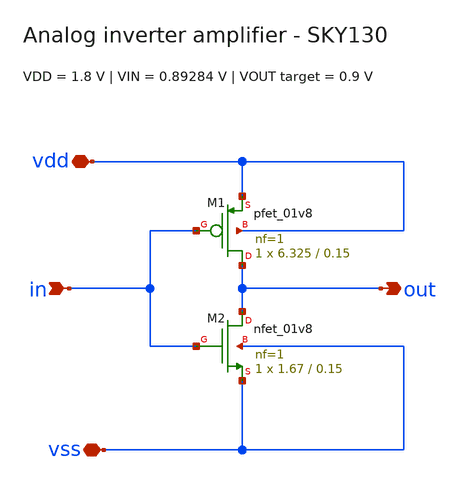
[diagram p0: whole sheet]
** sch_path: ISSCC27/submitted_notebooks/PerfPDN/examples/inverter_amplifier/inv.sch
**.subckt inv in out vdd vss
*.ipin in
*.opin out
*.iopin vdd
*.iopin vss
XM1 out in vdd vdd sky130_fd_pr__pfet_01v8 L=0.15 W=6.325 nf=1 ad='int(( 1 + 1 ) / 2 ) * 6.325 / 1 * 0.29'
+ as='int(( 1 + 2 ) / 2 ) * 6.325 / 1 * 0.29' pd='2 * int(( 1 + 1 ) / 2 ) * ( 6.325 / 1 + 0.29 )' ps='2 * int(( 1 + 2 ) / 2 ) * ( 6.325 / 1 + 0.29 )'
+ nrd='0.29 / 6.325 ' nrs='0.29 / 6.325 ' sa=0 sb=0 sd=0 mult=1 m=1
XM2 out in vss vss sky130_fd_pr__nfet_01v8 L=0.15 W=1.67 nf=1 ad='int(( 1 + 1 ) / 2 ) * 1.67 / 1 * 0.29'
+ as='int(( 1 + 2 ) / 2 ) * 1.67 / 1 * 0.29' pd='2 * int(( 1 + 1 ) / 2 ) * ( 1.67 / 1 + 0.29 )' ps='2 * int(( 1 + 2 ) / 2 ) * ( 1.67 / 1 + 0.29 )'
+ nrd='0.29 / 1.67 ' nrs='0.29 / 1.67 ' sa=0 sb=0 sd=0 mult=1 m=1
**.ends
.end
